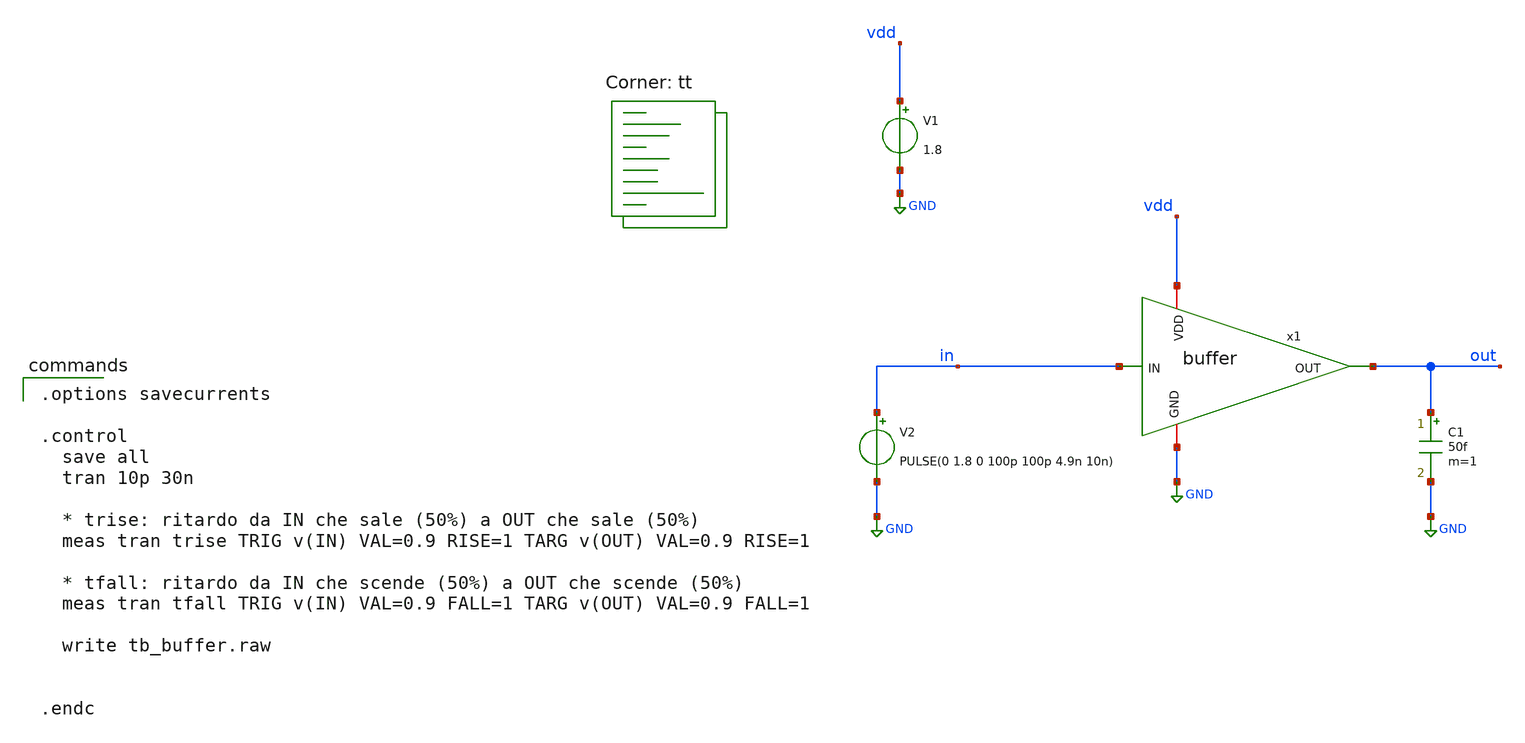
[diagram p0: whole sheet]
** sch_path: 03_magic_layout/soluzioni/lab02/xschem/tb_buffer.sch
**.subckt tb_buffer
x1 vdd GND out in buffer
V1 vdd GND 1.8
V2 in GND PULSE(0 1.8 0 100p 100p 4.9n 10n)
C1 out GND 50f m=1
**** begin user architecture code
.lib $::SKYWATER_MODELS/sky130.lib.spice tt

.options savecurrents

.control
  save all
  tran 10p 30n

  * trise: ritardo da IN che sale (50%) a OUT che sale (50%)
  meas tran trise TRIG v(IN) VAL=0.9 RISE=1 TARG v(OUT) VAL=0.9 RISE=1

  * tfall: ritardo da IN che scende (50%) a OUT che scende (50%)
  meas tran tfall TRIG v(IN) VAL=0.9 FALL=1 TARG v(OUT) VAL=0.9 FALL=1

  write tb_buffer.raw


.endc

**** end user architecture code
**.ends
.GLOBAL GND
.end
